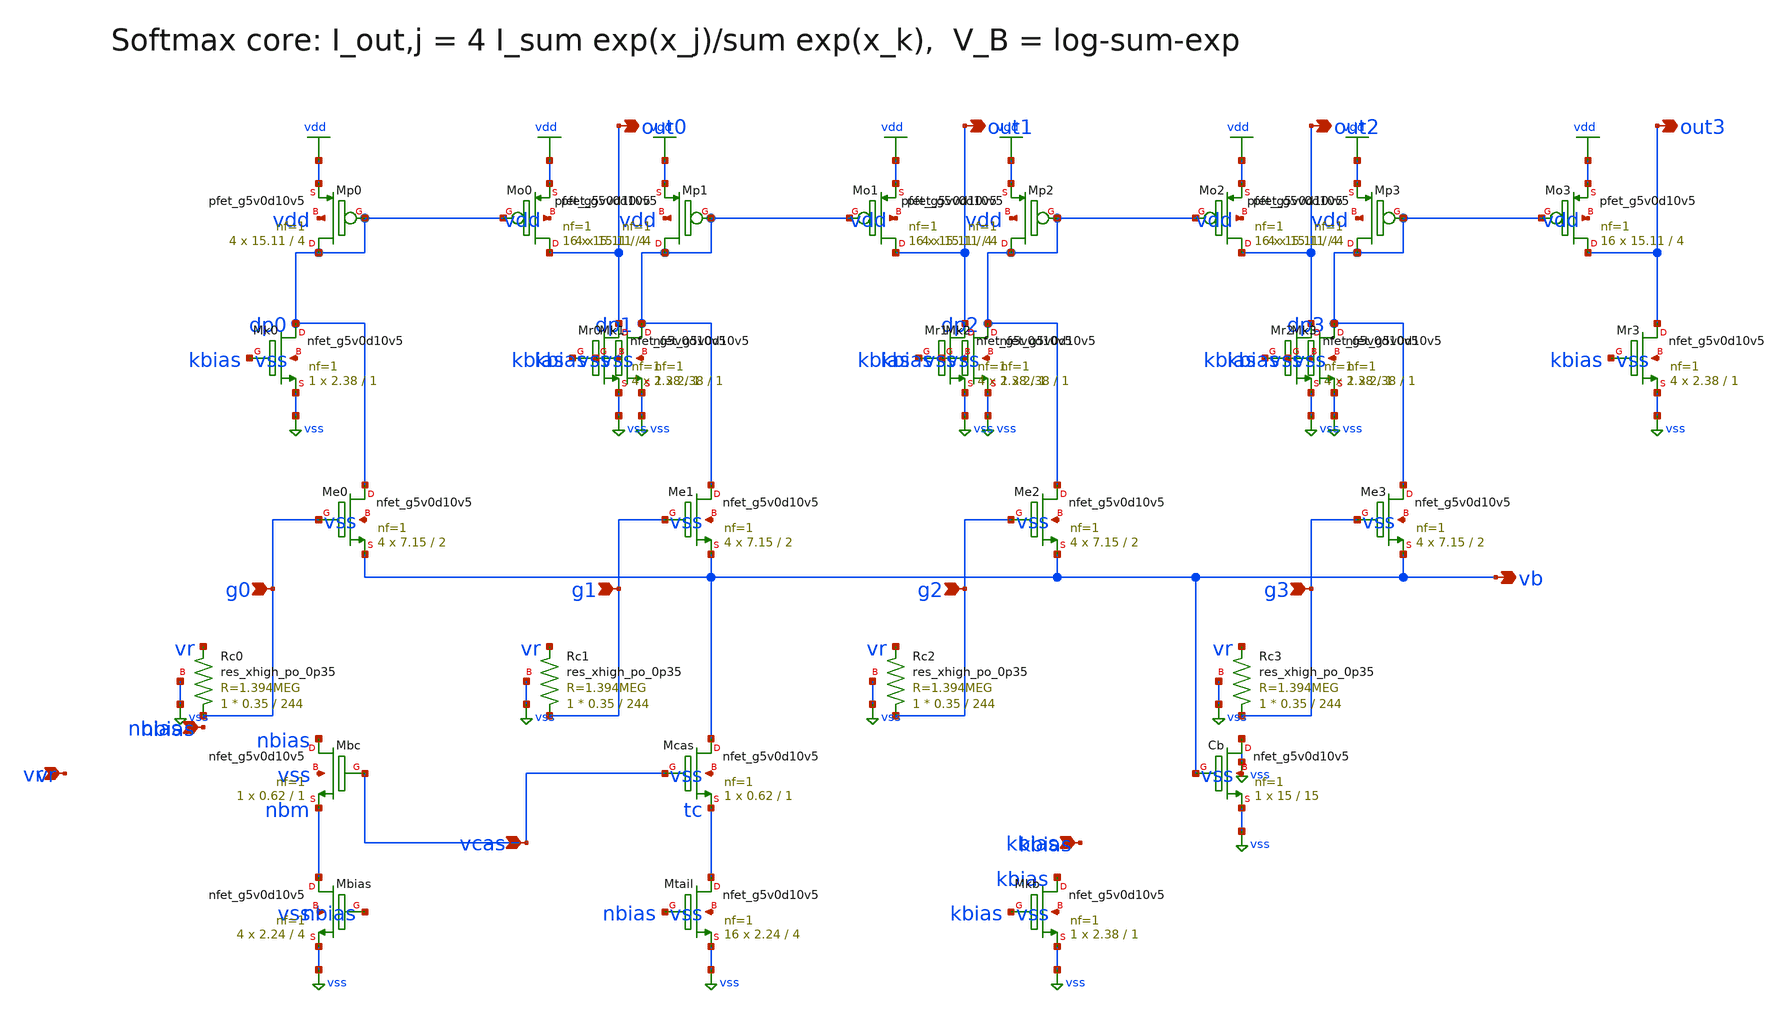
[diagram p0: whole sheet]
** sch_path: xschem/rt5w_softmax.sch
**.subckt rt5w_softmax g0 out0 g1 out1 g2 out2 g3 out3 nbias vcas kbias vr vb
*.ipin g0
*.opin out0
*.ipin g1
*.opin out1
*.ipin g2
*.opin out2
*.ipin g3
*.opin out3
*.ipin nbias
*.ipin vcas
*.ipin kbias
*.ipin vr
*.opin vb
XMp0 dp0 dp0 vdd vdd sky130_fd_pr__pfet_g5v0d10v5 L=4 W=15.11 nf=1 ad=4.382 as=4.382 pd=30.8 ps=30.8
+ nrd=0.01919 nrs=0.01919 sa=0 sb=0 sd=0 mult=4 m=4
XMo0 out0 dp0 vdd vdd sky130_fd_pr__pfet_g5v0d10v5 L=4 W=15.11 nf=1 ad=4.382 as=4.382 pd=30.8
+ ps=30.8 nrd=0.01919 nrs=0.01919 sa=0 sb=0 sd=0 mult=16 m=16
XMk0 dp0 kbias vss vss sky130_fd_pr__nfet_g5v0d10v5 L=1 W=2.38 nf=1 ad=0.6902 as=0.6902 pd=5.34
+ ps=5.34 nrd=0.1218 nrs=0.1218 sa=0 sb=0 sd=0 mult=1 m=1
XMr0 out0 kbias vss vss sky130_fd_pr__nfet_g5v0d10v5 L=1 W=2.38 nf=1 ad=0.6902 as=0.6902 pd=5.34
+ ps=5.34 nrd=0.1218 nrs=0.1218 sa=0 sb=0 sd=0 mult=4 m=4
XMe0 dp0 g0 vb vss sky130_fd_pr__nfet_g5v0d10v5 L=2 W=7.15 nf=1 ad=2.074 as=2.074 pd=14.88 ps=14.88
+ nrd=0.04056 nrs=0.04056 sa=0 sb=0 sd=0 mult=4 m=4
XRc0 g0 vr vss sky130_fd_pr__res_xhigh_po_0p35 L=244 mult=1 m=1
XMp1 dp1 dp1 vdd vdd sky130_fd_pr__pfet_g5v0d10v5 L=4 W=15.11 nf=1 ad=4.382 as=4.382 pd=30.8 ps=30.8
+ nrd=0.01919 nrs=0.01919 sa=0 sb=0 sd=0 mult=4 m=4
XMo1 out1 dp1 vdd vdd sky130_fd_pr__pfet_g5v0d10v5 L=4 W=15.11 nf=1 ad=4.382 as=4.382 pd=30.8
+ ps=30.8 nrd=0.01919 nrs=0.01919 sa=0 sb=0 sd=0 mult=16 m=16
XMk1 dp1 kbias vss vss sky130_fd_pr__nfet_g5v0d10v5 L=1 W=2.38 nf=1 ad=0.6902 as=0.6902 pd=5.34
+ ps=5.34 nrd=0.1218 nrs=0.1218 sa=0 sb=0 sd=0 mult=1 m=1
XMr1 out1 kbias vss vss sky130_fd_pr__nfet_g5v0d10v5 L=1 W=2.38 nf=1 ad=0.6902 as=0.6902 pd=5.34
+ ps=5.34 nrd=0.1218 nrs=0.1218 sa=0 sb=0 sd=0 mult=4 m=4
XMe1 dp1 g1 vb vss sky130_fd_pr__nfet_g5v0d10v5 L=2 W=7.15 nf=1 ad=2.074 as=2.074 pd=14.88 ps=14.88
+ nrd=0.04056 nrs=0.04056 sa=0 sb=0 sd=0 mult=4 m=4
XRc1 g1 vr vss sky130_fd_pr__res_xhigh_po_0p35 L=244 mult=1 m=1
XMp2 dp2 dp2 vdd vdd sky130_fd_pr__pfet_g5v0d10v5 L=4 W=15.11 nf=1 ad=4.382 as=4.382 pd=30.8 ps=30.8
+ nrd=0.01919 nrs=0.01919 sa=0 sb=0 sd=0 mult=4 m=4
XMo2 out2 dp2 vdd vdd sky130_fd_pr__pfet_g5v0d10v5 L=4 W=15.11 nf=1 ad=4.382 as=4.382 pd=30.8
+ ps=30.8 nrd=0.01919 nrs=0.01919 sa=0 sb=0 sd=0 mult=16 m=16
XMk2 dp2 kbias vss vss sky130_fd_pr__nfet_g5v0d10v5 L=1 W=2.38 nf=1 ad=0.6902 as=0.6902 pd=5.34
+ ps=5.34 nrd=0.1218 nrs=0.1218 sa=0 sb=0 sd=0 mult=1 m=1
XMr2 out2 kbias vss vss sky130_fd_pr__nfet_g5v0d10v5 L=1 W=2.38 nf=1 ad=0.6902 as=0.6902 pd=5.34
+ ps=5.34 nrd=0.1218 nrs=0.1218 sa=0 sb=0 sd=0 mult=4 m=4
XMe2 dp2 g2 vb vss sky130_fd_pr__nfet_g5v0d10v5 L=2 W=7.15 nf=1 ad=2.074 as=2.074 pd=14.88 ps=14.88
+ nrd=0.04056 nrs=0.04056 sa=0 sb=0 sd=0 mult=4 m=4
XRc2 g2 vr vss sky130_fd_pr__res_xhigh_po_0p35 L=244 mult=1 m=1
XMp3 dp3 dp3 vdd vdd sky130_fd_pr__pfet_g5v0d10v5 L=4 W=15.11 nf=1 ad=4.382 as=4.382 pd=30.8 ps=30.8
+ nrd=0.01919 nrs=0.01919 sa=0 sb=0 sd=0 mult=4 m=4
XMo3 out3 dp3 vdd vdd sky130_fd_pr__pfet_g5v0d10v5 L=4 W=15.11 nf=1 ad=4.382 as=4.382 pd=30.8
+ ps=30.8 nrd=0.01919 nrs=0.01919 sa=0 sb=0 sd=0 mult=16 m=16
XMk3 dp3 kbias vss vss sky130_fd_pr__nfet_g5v0d10v5 L=1 W=2.38 nf=1 ad=0.6902 as=0.6902 pd=5.34
+ ps=5.34 nrd=0.1218 nrs=0.1218 sa=0 sb=0 sd=0 mult=1 m=1
XMr3 out3 kbias vss vss sky130_fd_pr__nfet_g5v0d10v5 L=1 W=2.38 nf=1 ad=0.6902 as=0.6902 pd=5.34
+ ps=5.34 nrd=0.1218 nrs=0.1218 sa=0 sb=0 sd=0 mult=4 m=4
XMe3 dp3 g3 vb vss sky130_fd_pr__nfet_g5v0d10v5 L=2 W=7.15 nf=1 ad=2.074 as=2.074 pd=14.88 ps=14.88
+ nrd=0.04056 nrs=0.04056 sa=0 sb=0 sd=0 mult=4 m=4
XRc3 g3 vr vss sky130_fd_pr__res_xhigh_po_0p35 L=244 mult=1 m=1
XMcas vb vcas tc vss sky130_fd_pr__nfet_g5v0d10v5 L=1 W=0.62 nf=1 ad=0.1798 as=0.1798 pd=1.82
+ ps=1.82 nrd=0.4677 nrs=0.4677 sa=0 sb=0 sd=0 mult=1 m=1
XMtail tc nbias vss vss sky130_fd_pr__nfet_g5v0d10v5 L=4 W=2.24 nf=1 ad=0.6496 as=0.6496 pd=5.06
+ ps=5.06 nrd=0.1295 nrs=0.1295 sa=0 sb=0 sd=0 mult=16 m=16
XMbc nbias vcas nbm vss sky130_fd_pr__nfet_g5v0d10v5 L=1 W=0.62 nf=1 ad=0.1798 as=0.1798 pd=1.82
+ ps=1.82 nrd=0.4677 nrs=0.4677 sa=0 sb=0 sd=0 mult=1 m=1
XMbias nbm nbias vss vss sky130_fd_pr__nfet_g5v0d10v5 L=4 W=2.24 nf=1 ad=0.6496 as=0.6496 pd=5.06
+ ps=5.06 nrd=0.1295 nrs=0.1295 sa=0 sb=0 sd=0 mult=4 m=4
XMkb kbias kbias vss vss sky130_fd_pr__nfet_g5v0d10v5 L=1 W=2.38 nf=1 ad=0.6902 as=0.6902 pd=5.34
+ ps=5.34 nrd=0.1218 nrs=0.1218 sa=0 sb=0 sd=0 mult=1 m=1
XCb vss vb vss vss sky130_fd_pr__nfet_g5v0d10v5 L=15 W=15 nf=1 ad=4.35 as=4.35 pd=30.58 ps=30.58
+ nrd=0.01933 nrs=0.01933 sa=0 sb=0 sd=0 mult=1 m=1
**.ends
.GLOBAL vdd
.GLOBAL vss
.end
